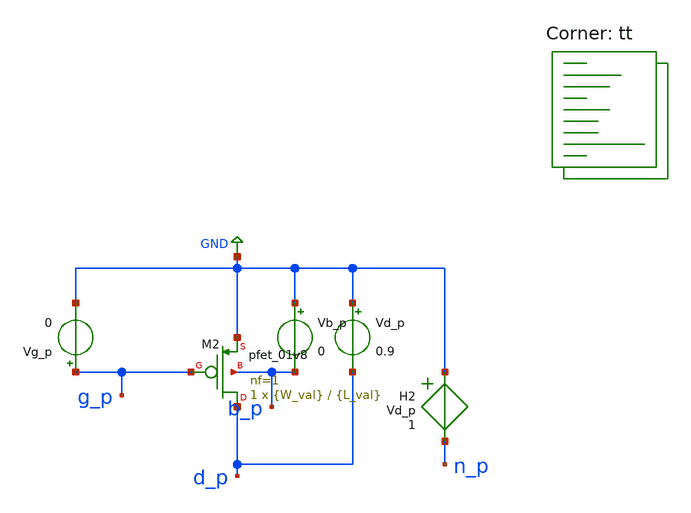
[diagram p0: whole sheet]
** sch_path: xschem/untitled-1.sch
**.subckt untitled-1
XM2 d_p g_p GND b_p sky130_fd_pr__pfet_01v8 L={L_val} W={W_val} nf=1 ad='int((1 + 1)/2) * {W_val} / 1 * 0.29'
+ as='int((1 + 2)/2) * {W_val} / 1 * 0.29' pd='2*int((1 + 1)/2) * ({W_val} / 1 + 0.29)' ps='2*int((1 + 2)/2) * ({W_val} / 1 + 0.29)'
+ nrd='0.29 / {W_val} ' nrs='0.29 / {W_val} ' sa=0 sb=0 sd=0 mult=1 m=1
H2 GND n_p Vd_p 1
Vg_p g_p GND 0
Vd_p GND d_p 0.9
Vb_p GND b_p 0
**** begin user architecture code


* gm/ID Characterization for Sky130 nfet_01v8
* Parameters
.param W_val = 10
.param L_val = 0.5
.dc Vg_n 0 1.8 0.01

.save all @m.xm1.msky130_fd_pr__nfet_01v8[id]
.save @m.xm1.msky130_fd_pr__nfet_01v8[vth]
.save @m.xm1.msky130_fd_pr__nfet_01v8[gm]
.save @m.xm1.msky130_fd_pr__nfet_01v8[cgg]
.save @m.xm1.msky130_fd_pr__nfet_01v8[w]
.save @m.xm1.msky130_fd_pr__nfet_01v8[l]
.save @m.xm1.msky130_fd_pr__nfet_01v8[gds]


.control

  * Direct Plotting in ngspice
  set xbrushwidth=2
 * set plot_vov = ' '
 * set plot_gm_id = ' '
 * set plot_id_W = ' '
 * set plot_gm_gmds = ' '
 * set plot_fT =' '

 foreach val 0.8 1.0 1.5 2.0
  run
  let W_n = @m.xm1.msky130_fd_pr__nfet_01v8[w]
  let L_n = @m.xm1.msky130_fd_pr__nfet_01v8[l]
  let g_m_n = @m.xm1.msky130_fd_pr__nfet_01v8[gm]
  let i_d_n = @m.xm1.msky130_fd_pr__nfet_01v8[id]
  let v_th_n = @m.xm1.msky130_fd_pr__nfet_01v8[vth]
  let c_gg_n =  @m.xm1.msky130_fd_pr__nfet_01v8[cgg]
  let g_ds_n =  @m.xm1.msky130_fd_pr__nfet_01v8[gds]


  let gm_id_n = 'g_m_n/i_d_n'
  let v_ov_n = 'v(g_n) - v_th_n'

  let w_T_n = 'g_m_n/c_gg_n'
  let f_T_n = 'w_T_n/('2*pi')'

  let gm_gmds_n = 'g_m_n/g_ds_n'

  let id_W_n = 'i_d_n/W_n'

  alterparam L_val = $val
  reset
 end
   print dc1.L dc2.L dc3.L
  *plot $plot_id_W vs $plot_gm_id ylog xlabel 'Current Eff S/A' ylabel 'A/W' title 'NMOS Id/W vs gm/Id'
  *plot $plot_gm_gmds vs $plot_gm_id xlabel 'Current Eff S/A' ylabel 'Intrinsic Gain' title 'NMOS gm/Id vs gm/gds'
  *plot $plot_fT vs $plot_gm_id xlabel 'Current Eff S/A' ylabel 'Transit Frequency GHz' title 'NMOS Id/W vs fT'
  *plot $plot_gm_id vs $plot_vov xlabel 'Overdrive Voltage V' ylabel 'Current Eff S/A' title 'NMOS gm/Id vs Vov'

  plot dc1.id_W_n vs dc1.gm_id_n dc2.id_W_n vs dc2.gm_id_n dc3.id_W_n vs dc3.gm_id_n  ylog xlabel 'Current Eff S/A'
+ ylabel 'A/W' title 'NMOS Id/W vs gm/Id'
  plot dc1.gm_gmds_n vs dc1.gm_id_n dc2.gm_gmds_n vs dc2.gm_id_n dc3.gm_gmds_n vs dc3.gm_id_n xlabel
+ 'Current Eff S/A' ylabel 'Intrinsic Gain' title 'NMOS gm/Id vs gm/gds'
  plot dc1.f_T_n vs dc1.gm_id_n dc2.f_T_n vs dc2.gm_id_n dc3.f_T_n vs dc3.gm_id_n xlabel 'Current Eff S/A'
+ ylabel 'Transit Frequency GHz' title 'NMOS Id/W vs fT'
  *plot $plot_gm_id vs $plot_vov xlabel 'Overdrive Voltage V' ylabel 'Current Eff S/A' title 'NMOS gm/Id vs Vov'

  plot dc1.id_W_p vs dc1.gm_id_p dc2.id_W_p vs dc2.gm_id_p dc3.id_W_p vs dc3.gm_id_p  ylog xlabel 'Current Eff S/A'
+ ylabel 'A/W' title 'PMOS Id/W vs gm/Id'
  plot dc1.gm_gmds_p vs dc1.gm_id_p dc2.gm_gmds_p vs dc2.gm_id_p dc3.gm_gmds_p vs dc3.gm_id_p xlabel
+ 'Current Eff S/A' ylabel 'Intrinsic Gain' title 'PMOS gm/Id vs gm/gds'
  plot dc1.f_T_p vs dc1.gm_id_p dc2.f_T_p vs dc2.gm_id_p dc3.f_T_p vs dc3.gm_id_p xlabel 'Current Eff S/A'
+ ylabel 'Transit Frequency GHz' title 'PMOS Id/W vs fT'

.endc
.end

.lib $::SKYWATER_MODELS/sky130.lib.spice tt
**** end user architecture code
**.ends
.GLOBAL GND
.end
